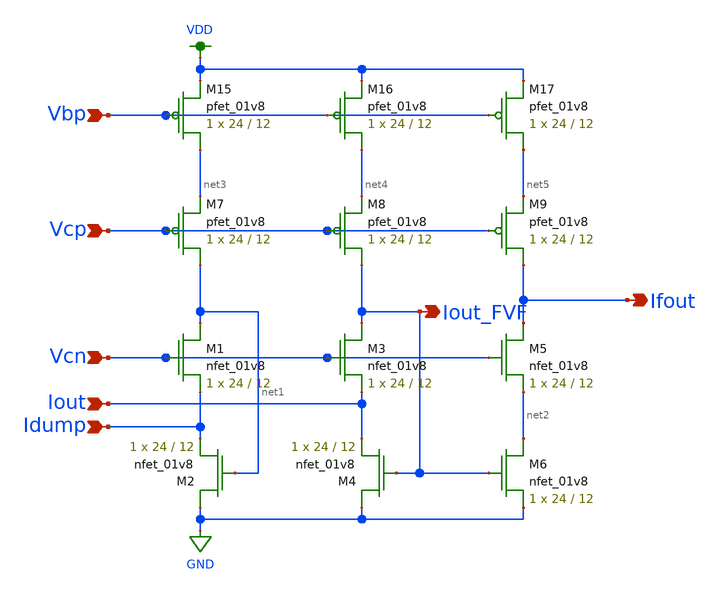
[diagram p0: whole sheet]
** sch_path: xschem/FVF-1.sch
**.subckt FVF-1 Vcn Iout Idump Vcp Vbp Ifout Iout_FVF
*.ipin Vcn
*.ipin Iout
*.ipin Idump
*.ipin Vcp
*.ipin Vbp
*.opin Ifout
*.opin Iout_FVF
XM1 net1 Vcn Idump GND sky130_fd_pr__nfet_01v8 L=12 W=24 nf=1 ad='int((nf+1)/2) * W/nf * 0.29' as='int((nf+2)/2) * W/nf * 0.29'
+ pd='2*int((nf+1)/2) * (W/nf + 0.29)' ps='2*int((nf+2)/2) * (W/nf + 0.29)' nrd='0.29 / W' nrs='0.29 / W'
+ sa=0 sb=0 sd=0 mult=1 m=1
XM2 GND net1 Idump GND sky130_fd_pr__nfet_01v8 L=12 W=24 nf=1 ad='int((nf+1)/2) * W/nf * 0.29' as='int((nf+2)/2) * W/nf * 0.29'
+ pd='2*int((nf+1)/2) * (W/nf + 0.29)' ps='2*int((nf+2)/2) * (W/nf + 0.29)' nrd='0.29 / W' nrs='0.29 / W'
+ sa=0 sb=0 sd=0 mult=1 m=1
XM3 Iout_FVF Vcn Iout GND sky130_fd_pr__nfet_01v8 L=12 W=24 nf=1 ad='int((nf+1)/2) * W/nf * 0.29' as='int((nf+2)/2) * W/nf * 0.29'
+ pd='2*int((nf+1)/2) * (W/nf + 0.29)' ps='2*int((nf+2)/2) * (W/nf + 0.29)' nrd='0.29 / W' nrs='0.29 / W'
+ sa=0 sb=0 sd=0 mult=1 m=1
XM4 GND Iout_FVF Iout GND sky130_fd_pr__nfet_01v8 L=12 W=24 nf=1 ad='int((nf+1)/2) * W/nf * 0.29' as='int((nf+2)/2) * W/nf * 0.29'
+ pd='2*int((nf+1)/2) * (W/nf + 0.29)' ps='2*int((nf+2)/2) * (W/nf + 0.29)' nrd='0.29 / W' nrs='0.29 / W'
+ sa=0 sb=0 sd=0 mult=1 m=1
XM5 Ifout Vcn net2 GND sky130_fd_pr__nfet_01v8 L=12 W=24 nf=1 ad='int((nf+1)/2) * W/nf * 0.29' as='int((nf+2)/2) * W/nf * 0.29'
+ pd='2*int((nf+1)/2) * (W/nf + 0.29)' ps='2*int((nf+2)/2) * (W/nf + 0.29)' nrd='0.29 / W' nrs='0.29 / W'
+ sa=0 sb=0 sd=0 mult=1 m=1
XM6 net2 Iout_FVF GND GND sky130_fd_pr__nfet_01v8 L=12 W=24 nf=1 ad='int((nf+1)/2) * W/nf * 0.29' as='int((nf+2)/2) * W/nf * 0.29'
+ pd='2*int((nf+1)/2) * (W/nf + 0.29)' ps='2*int((nf+2)/2) * (W/nf + 0.29)' nrd='0.29 / W' nrs='0.29 / W'
+ sa=0 sb=0 sd=0 mult=1 m=1
XM7 net1 Vcp net3 VDD sky130_fd_pr__pfet_01v8 L=12 W=24 nf=1 ad='int((nf+1)/2) * W/nf * 0.29' as='int((nf+2)/2) * W/nf * 0.29'
+ pd='2*int((nf+1)/2) * (W/nf + 0.29)' ps='2*int((nf+2)/2) * (W/nf + 0.29)' nrd='0.29 / W' nrs='0.29 / W'
+ sa=0 sb=0 sd=0 mult=1 m=1
XM8 Iout_FVF Vcp net4 VDD sky130_fd_pr__pfet_01v8 L=12 W=24 nf=1 ad='int((nf+1)/2) * W/nf * 0.29' as='int((nf+2)/2) * W/nf * 0.29'
+ pd='2*int((nf+1)/2) * (W/nf + 0.29)' ps='2*int((nf+2)/2) * (W/nf + 0.29)' nrd='0.29 / W' nrs='0.29 / W'
+ sa=0 sb=0 sd=0 mult=1 m=1
XM9 Ifout Vcp net5 VDD sky130_fd_pr__pfet_01v8 L=12 W=24 nf=1 ad='int((nf+1)/2) * W/nf * 0.29' as='int((nf+2)/2) * W/nf * 0.29'
+ pd='2*int((nf+1)/2) * (W/nf + 0.29)' ps='2*int((nf+2)/2) * (W/nf + 0.29)' nrd='0.29 / W' nrs='0.29 / W'
+ sa=0 sb=0 sd=0 mult=1 m=1
XM15 net3 Vbp VDD VDD sky130_fd_pr__pfet_01v8 L=12 W=24 nf=1 ad='int((nf+1)/2) * W/nf * 0.29' as='int((nf+2)/2) * W/nf * 0.29'
+ pd='2*int((nf+1)/2) * (W/nf + 0.29)' ps='2*int((nf+2)/2) * (W/nf + 0.29)' nrd='0.29 / W' nrs='0.29 / W'
+ sa=0 sb=0 sd=0 mult=1 m=1
XM16 net4 Vbp VDD VDD sky130_fd_pr__pfet_01v8 L=12 W=24 nf=1 ad='int((nf+1)/2) * W/nf * 0.29' as='int((nf+2)/2) * W/nf * 0.29'
+ pd='2*int((nf+1)/2) * (W/nf + 0.29)' ps='2*int((nf+2)/2) * (W/nf + 0.29)' nrd='0.29 / W' nrs='0.29 / W'
+ sa=0 sb=0 sd=0 mult=1 m=1
XM17 net5 Vbp VDD VDD sky130_fd_pr__pfet_01v8 L=12 W=24 nf=1 ad='int((nf+1)/2) * W/nf * 0.29' as='int((nf+2)/2) * W/nf * 0.29'
+ pd='2*int((nf+1)/2) * (W/nf + 0.29)' ps='2*int((nf+2)/2) * (W/nf + 0.29)' nrd='0.29 / W' nrs='0.29 / W'
+ sa=0 sb=0 sd=0 mult=1 m=1
**.ends
.GLOBAL VDD
.GLOBAL GND
.end
